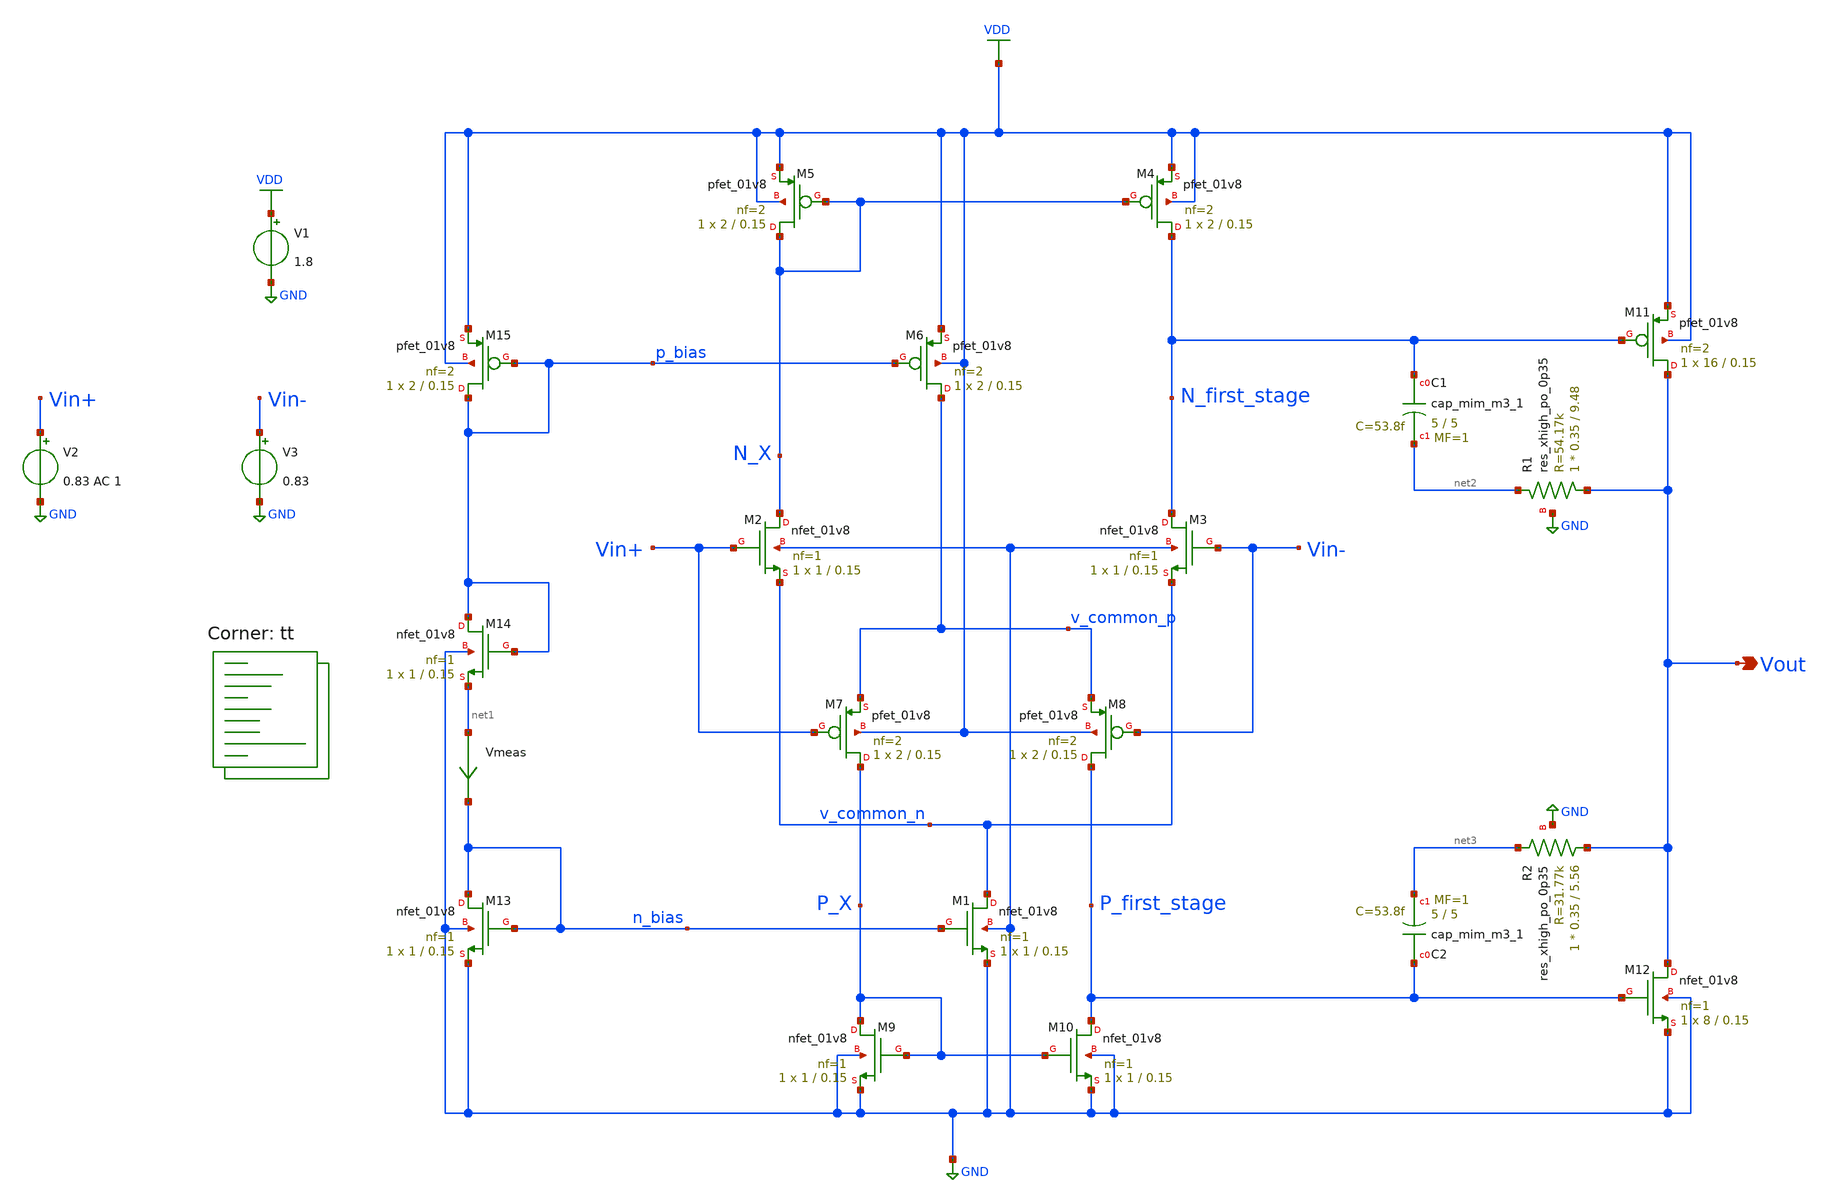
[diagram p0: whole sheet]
** sch_path: projects/pll/charge_pump/xschem_ngspice/tb_rail_to_rail_opamp6_DC.sch
**.subckt tb_rail_to_rail_opamp6_DC Vout
*.opin Vout
V1 VDD GND 1.8
V2 Vin+ GND 0.83 AC 1
V3 Vin- GND 0.83
XM2 N_X Vin+ v_common_n GND sky130_fd_pr__nfet_01v8 L=0.15 W=1 nf=1 ad='int((nf+1)/2) * W/nf * 0.29'
+ as='int((nf+2)/2) * W/nf * 0.29' pd='2*int((nf+1)/2) * (W/nf + 0.29)' ps='2*int((nf+2)/2) * (W/nf + 0.29)'
+ nrd='0.29 / W' nrs='0.29 / W' sa=0 sb=0 sd=0 mult=1 m=1
XM3 N_first_stage Vin- v_common_n GND sky130_fd_pr__nfet_01v8 L=0.15 W=1 nf=1 ad='int((nf+1)/2) * W/nf * 0.29'
+ as='int((nf+2)/2) * W/nf * 0.29' pd='2*int((nf+1)/2) * (W/nf + 0.29)' ps='2*int((nf+2)/2) * (W/nf + 0.29)'
+ nrd='0.29 / W' nrs='0.29 / W' sa=0 sb=0 sd=0 mult=1 m=1
XM5 N_X N_X VDD VDD sky130_fd_pr__pfet_01v8 L=0.15 W=2 nf=2 ad='int((nf+1)/2) * W/nf * 0.29' as='int((nf+2)/2) * W/nf * 0.29'
+ pd='2*int((nf+1)/2) * (W/nf + 0.29)' ps='2*int((nf+2)/2) * (W/nf + 0.29)' nrd='0.29 / W' nrs='0.29 / W'
+ sa=0 sb=0 sd=0 mult=1 m=1
XM4 N_first_stage N_X VDD VDD sky130_fd_pr__pfet_01v8 L=0.15 W=2 nf=2 ad='int((nf+1)/2) * W/nf * 0.29'
+ as='int((nf+2)/2) * W/nf * 0.29' pd='2*int((nf+1)/2) * (W/nf + 0.29)' ps='2*int((nf+2)/2) * (W/nf + 0.29)'
+ nrd='0.29 / W' nrs='0.29 / W' sa=0 sb=0 sd=0 mult=1 m=1
XM6 v_common_p p_bias VDD VDD sky130_fd_pr__pfet_01v8 L=0.15 W=2 nf=2 ad='int((nf+1)/2) * W/nf * 0.29'
+ as='int((nf+2)/2) * W/nf * 0.29' pd='2*int((nf+1)/2) * (W/nf + 0.29)' ps='2*int((nf+2)/2) * (W/nf + 0.29)'
+ nrd='0.29 / W' nrs='0.29 / W' sa=0 sb=0 sd=0 mult=1 m=1
XM7 P_X Vin+ v_common_p VDD sky130_fd_pr__pfet_01v8 L=0.15 W=2 nf=2 ad='int((nf+1)/2) * W/nf * 0.29'
+ as='int((nf+2)/2) * W/nf * 0.29' pd='2*int((nf+1)/2) * (W/nf + 0.29)' ps='2*int((nf+2)/2) * (W/nf + 0.29)'
+ nrd='0.29 / W' nrs='0.29 / W' sa=0 sb=0 sd=0 mult=1 m=1
XM8 P_first_stage Vin- v_common_p VDD sky130_fd_pr__pfet_01v8 L=0.15 W=2 nf=2 ad='int((nf+1)/2) * W/nf * 0.29'
+ as='int((nf+2)/2) * W/nf * 0.29' pd='2*int((nf+1)/2) * (W/nf + 0.29)' ps='2*int((nf+2)/2) * (W/nf + 0.29)'
+ nrd='0.29 / W' nrs='0.29 / W' sa=0 sb=0 sd=0 mult=1 m=1
XM9 P_X P_X GND GND sky130_fd_pr__nfet_01v8 L=0.15 W=1 nf=1 ad='int((nf+1)/2) * W/nf * 0.29' as='int((nf+2)/2) * W/nf * 0.29'
+ pd='2*int((nf+1)/2) * (W/nf + 0.29)' ps='2*int((nf+2)/2) * (W/nf + 0.29)' nrd='0.29 / W' nrs='0.29 / W'
+ sa=0 sb=0 sd=0 mult=1 m=1
XM10 P_first_stage P_X GND GND sky130_fd_pr__nfet_01v8 L=0.15 W=1 nf=1 ad='int((nf+1)/2) * W/nf * 0.29'
+ as='int((nf+2)/2) * W/nf * 0.29' pd='2*int((nf+1)/2) * (W/nf + 0.29)' ps='2*int((nf+2)/2) * (W/nf + 0.29)'
+ nrd='0.29 / W' nrs='0.29 / W' sa=0 sb=0 sd=0 mult=1 m=1
XM1 v_common_n n_bias GND GND sky130_fd_pr__nfet_01v8 L=0.15 W=1 nf=1 ad='int((nf+1)/2) * W/nf * 0.29'
+ as='int((nf+2)/2) * W/nf * 0.29' pd='2*int((nf+1)/2) * (W/nf + 0.29)' ps='2*int((nf+2)/2) * (W/nf + 0.29)'
+ nrd='0.29 / W' nrs='0.29 / W' sa=0 sb=0 sd=0 mult=1 m=1
XM11 Vout N_first_stage VDD VDD sky130_fd_pr__pfet_01v8 L=0.15 W=16 nf=2 ad='int((nf+1)/2) * W/nf * 0.29'
+ as='int((nf+2)/2) * W/nf * 0.29' pd='2*int((nf+1)/2) * (W/nf + 0.29)' ps='2*int((nf+2)/2) * (W/nf + 0.29)'
+ nrd='0.29 / W' nrs='0.29 / W' sa=0 sb=0 sd=0 mult=1 m=1
XM12 Vout P_first_stage GND GND sky130_fd_pr__nfet_01v8 L=0.15 W=8 nf=1 ad='int((nf+1)/2) * W/nf * 0.29'
+ as='int((nf+2)/2) * W/nf * 0.29' pd='2*int((nf+1)/2) * (W/nf + 0.29)' ps='2*int((nf+2)/2) * (W/nf + 0.29)'
+ nrd='0.29 / W' nrs='0.29 / W' sa=0 sb=0 sd=0 mult=1 m=1
XM13 n_bias n_bias GND GND sky130_fd_pr__nfet_01v8 L=0.15 W=1 nf=1 ad='int((nf+1)/2) * W/nf * 0.29' as='int((nf+2)/2) * W/nf * 0.29'
+ pd='2*int((nf+1)/2) * (W/nf + 0.29)' ps='2*int((nf+2)/2) * (W/nf + 0.29)' nrd='0.29 / W' nrs='0.29 / W'
+ sa=0 sb=0 sd=0 mult=1 m=1
XM15 p_bias p_bias VDD VDD sky130_fd_pr__pfet_01v8 L=0.15 W=2 nf=2 ad='int((nf+1)/2) * W/nf * 0.29' as='int((nf+2)/2) * W/nf * 0.29'
+ pd='2*int((nf+1)/2) * (W/nf + 0.29)' ps='2*int((nf+2)/2) * (W/nf + 0.29)' nrd='0.29 / W' nrs='0.29 / W'
+ sa=0 sb=0 sd=0 mult=1 m=1
Vmeas net1 n_bias 0
.save i(vmeas)
XM14 p_bias p_bias net1 GND sky130_fd_pr__nfet_01v8 L=0.15 W=1 nf=1 ad='int((nf+1)/2) * W/nf * 0.29'
+ as='int((nf+2)/2) * W/nf * 0.29' pd='2*int((nf+1)/2) * (W/nf + 0.29)' ps='2*int((nf+2)/2) * (W/nf + 0.29)'
+ nrd='0.29 / W' nrs='0.29 / W' sa=0 sb=0 sd=0 mult=1 m=1
XC1 N_first_stage net2 sky130_fd_pr__cap_mim_m3_1 W=5 L=5 MF=1 m=1
XC2 P_first_stage net3 sky130_fd_pr__cap_mim_m3_1 W=5 L=5 MF=1 m=1
XR1 Vout net2 GND sky130_fd_pr__res_xhigh_po_0p35 L=9.48 mult=1 m=1
XR2 Vout net3 GND sky130_fd_pr__res_xhigh_po_0p35 L=5.56 mult=1 m=1
**** begin user architecture code



.option wnflag=1
.option savecurrents


.save @m.xm1.msky130_fd_pr__nfet_01v8[gm] @m.xm2.msky130_fd_pr__nfet_01v8[gm] @m.xm3.msky130_fd_pr__nfet_01v8[gm] @m.xm4.msky130_fd_pr__pfet_01v8[gm] @m.xm5.msky130_fd_pr__pfet_01v8[gm] @m.xm6.msky130_fd_pr__pfet_01v8[gm] @m.xm7.msky130_fd_pr__pfet_01v8[gm] @m.xm8.msky130_fd_pr__pfet_01v8[gm] @m.xm9.msky130_fd_pr__nfet_01v8[gm] @m.xm10.msky130_fd_pr__nfet_01v8[gm] @m.xm11.msky130_fd_pr__pfet_01v8[gm] @m.xm12.msky130_fd_pr__nfet_01v8[gm] @m.xm13.msky130_fd_pr__nfet_01v8[gm] @m.xm14.msky130_fd_pr__nfet_01v8[gm] @m.xm15.msky130_fd_pr__pfet_01v8[gm]


.control
  save all
  * dc V3 0 1.8 0.01
  ac dec 20 1 1T
  * tran 100p 1u
  * write tb_rail_to_rail_opamp6_DC.raw
  write tb_rail_to_rail_opamp6_DC_2.raw
  set appendwrite
.endc



.lib $::SKYWATER_MODELS/sky130.lib.spice tt
**** end user architecture code
**.ends
.GLOBAL GND
.GLOBAL VDD
.end
